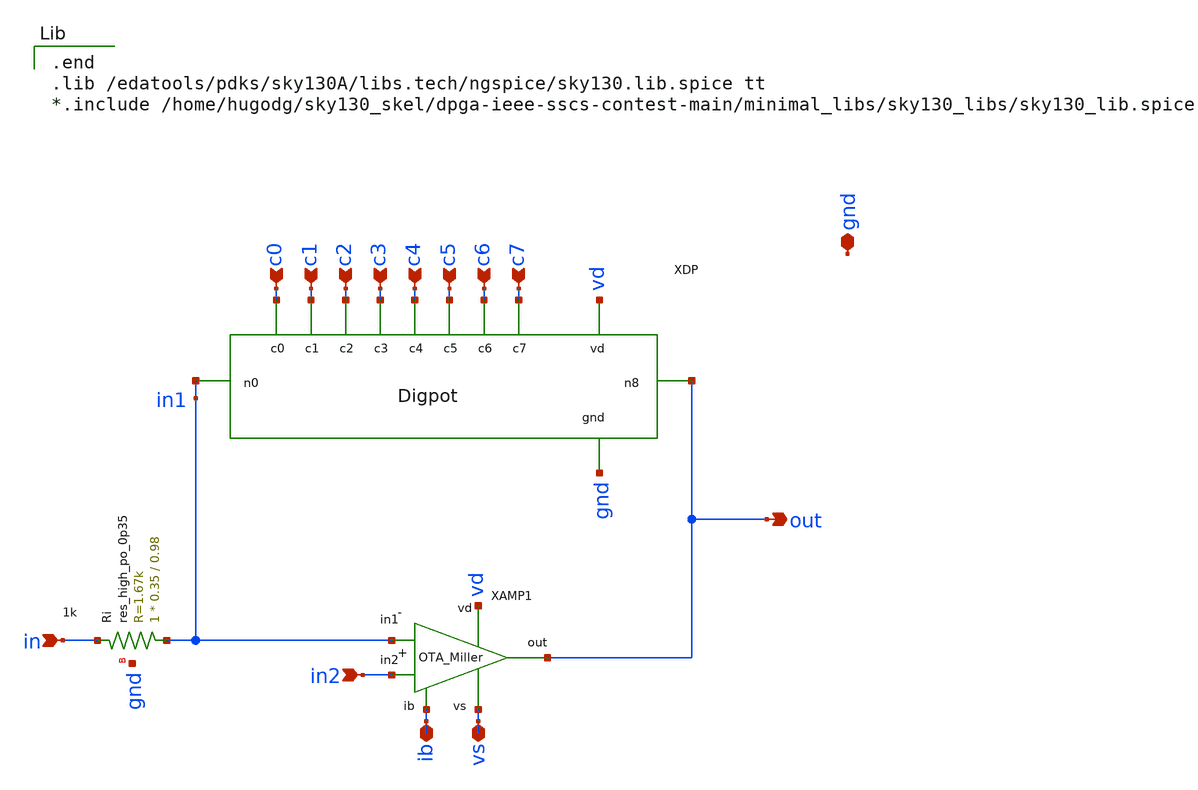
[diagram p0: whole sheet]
** sch_path: xschem/dpga.sch
* xschem/ota.sch:
* Copyright 2020 Stefan Frederik Schippers
* Licensed under the Apache License, Version 2.0 (the "License");
**.subckt dpga in in2 ib vs out gnd c0 c1 c2 c3 c4 c5 c6 c7
*.ipin in
*.ipin in2
*.iopin ib
*.iopin vs
*.opin out
*.iopin gnd
*.ipin c0
*.ipin c1
*.ipin c2
*.ipin c3
*.ipin c4
*.ipin c5
*.ipin c6
*.ipin c7
XDP1 gnd vd c5 c1 c2 c6 c7 c3 c0 c4 out in1 digpot
XOTA1 vd ib out in2 in1 vs ota
XRi in1 in gnd sky130_fd_pr__res_high_po_0p35 L=0.98 mult=1 m=1
**** begin user architecture code

.end
.lib /edatools/pdks/sky130A/libs.tech/ngspice/sky130.lib.spice tt
*.include /home/hugodg/sky130_skel/dpga-ieee-sscs-contest-main/minimal_libs/sky130_libs/sky130_lib.spice

**** end user architecture code
**.ends

* expanding   symbol:  /home/hugodg/sky130_skel/dpga-ieee-sscs-contest-main/xschem/digpot.sym # of
*+ pins=12
** sym_path: xschem/digpot.sym
** sch_path: xschem/digpot.sch
.subckt digpot gnd vd c5 c1 c2 c6 c7 c3 c0 c4 n8 n0
*.ipin c0
*.ipin c1
*.ipin c2
*.ipin c3
*.ipin c4
*.ipin c5
*.ipin c6
*.ipin c7
*.iopin gnd
*.iopin vd
*.iopin n0
*.iopin n8
xtg1 c0 vd n1 gnd n0 tg
xtg2 c1 vd n2 gnd n1 tg
xtg3 c2 vd n3 gnd n2 tg
xtg4 c3 vd n4 gnd n3 tg
xtg5 c4 vd n5 gnd n4 tg
xtg6 c5 vd n6 gnd n5 tg
xtg7 c6 vd n7 gnd n6 tg
xtg8 c7 vd n8 gnd n7 tg
XR0 n1 n0 gnd sky130_fd_pr__res_high_po_0p35 L=0.98 mult=1 m=1
XR1 n2 n1 gnd sky130_fd_pr__res_high_po_0p35 L=2.07 mult=1 m=1
XR2 n3 n2 gnd sky130_fd_pr__res_xhigh_po_0p35 L=0.58 mult=1 m=1
XR3 n4 n3 gnd sky130_fd_pr__res_xhigh_po_0p35 L=1.28 mult=1 m=1
XR4 n5 n4 gnd sky130_fd_pr__res_xhigh_po_0p35 L=2.68 mult=1 m=1
XR5 n6 n5 gnd sky130_fd_pr__res_xhigh_po_0p35 L=5.48 mult=1 m=1
XR6 n7 n6 gnd sky130_fd_pr__res_xhigh_po_0p35 L=10.73 mult=1 m=1
XR7 n8 n7 gnd sky130_fd_pr__res_xhigh_po_0p35 L=22.28 mult=1 m=1
.ends


* expanding   symbol:  /home/hugodg/sky130_skel/dpga-ieee-sscs-contest-main/xschem/ota.sym # of
*+ pins=6
** sym_path: xschem/ota.sym
** sch_path: xschem/ota.sch
.subckt ota vd ib out in2 in1 vs
*.iopin vd
*.iopin vs
*.iopin ib
*.ipin in1
*.ipin in2
*.opin out
XM4 d c vs vs sky130_fd_pr__nfet_01v8 L=1 W=0.861 nf=1 ad='int((nf+1)/2) * W/nf * 0.29' as='int((nf+2)/2) * W/nf * 0.29'
+ pd='2*int((nf+1)/2) * (W/nf + 0.29)' ps='2*int((nf+2)/2) * (W/nf + 0.29)' nrd='0.29 / W' nrs='0.29 / W'
+ sa=0 sb=0 sd=0 mult=1 m=1
XM7 e d vs vs sky130_fd_pr__nfet_01v8 L=1 W=8.61 nf=2 ad='int((nf+1)/2) * W/nf * 0.29' as='int((nf+2)/2) * W/nf * 0.29'
+ pd='2*int((nf+1)/2) * (W/nf + 0.29)' ps='2*int((nf+2)/2) * (W/nf + 0.29)' nrd='0.29 / W' nrs='0.29 / W'
+ sa=0 sb=0 sd=0 mult=1 m=1
XM5 ib ib vd vd sky130_fd_pr__pfet_01v8 L=1 W=5.85 nf=1 ad='int((nf+1)/2) * W/nf * 0.29' as='int((nf+2)/2) * W/nf * 0.29'
+ pd='2*int((nf+1)/2) * (W/nf + 0.29)' ps='2*int((nf+2)/2) * (W/nf + 0.29)' nrd='0.29 / W' nrs='0.29 / W'
+ sa=0 sb=0 sd=0 mult=1 m=1
XM6 b ib vd vd sky130_fd_pr__pfet_01v8 L=1 W=5.85 nf=1 ad='int((nf+1)/2) * W/nf * 0.29' as='int((nf+2)/2) * W/nf * 0.29'
+ pd='2*int((nf+1)/2) * (W/nf + 0.29)' ps='2*int((nf+2)/2) * (W/nf + 0.29)' nrd='0.29 / W' nrs='0.29 / W'
+ sa=0 sb=0 sd=0 mult=1 m=1
XM8 e ib vd vd sky130_fd_pr__pfet_01v8 L=1 W=29.3 nf=5 ad='int((nf+1)/2) * W/nf * 0.29' as='int((nf+2)/2) * W/nf * 0.29'
+ pd='2*int((nf+1)/2) * (W/nf + 0.29)' ps='2*int((nf+2)/2) * (W/nf + 0.29)' nrd='0.29 / W' nrs='0.29 / W'
+ sa=0 sb=0 sd=0 mult=1 m=1
XM10 out ib vd vd sky130_fd_pr__pfet_01v8 L=1 W=5.85 nf=1 ad='int((nf+1)/2) * W/nf * 0.29' as='int((nf+2)/2) * W/nf * 0.29'
+ pd='2*int((nf+1)/2) * (W/nf + 0.29)' ps='2*int((nf+2)/2) * (W/nf + 0.29)' nrd='0.29 / W' nrs='0.29 / W'
+ sa=0 sb=0 sd=0 mult=1 m=1
XM9 vs e out out sky130_fd_pr__pfet_01v8 L=1 W=5.85 nf=1 ad='int((nf+1)/2) * W/nf * 0.29' as='int((nf+2)/2) * W/nf * 0.29'
+ pd='2*int((nf+1)/2) * (W/nf + 0.29)' ps='2*int((nf+2)/2) * (W/nf + 0.29)' nrd='0.29 / W' nrs='0.29 / W'
+ sa=0 sb=0 sd=0 mult=1 m=1
XM1 c in1 b b sky130_fd_pr__pfet_01v8 L=1 W=2.93 nf=1 ad='int((nf+1)/2) * W/nf * 0.29' as='int((nf+2)/2) * W/nf * 0.29'
+ pd='2*int((nf+1)/2) * (W/nf + 0.29)' ps='2*int((nf+2)/2) * (W/nf + 0.29)' nrd='0.29 / W' nrs='0.29 / W'
+ sa=0 sb=0 sd=0 mult=1 m=1
XM2 d in2 b b sky130_fd_pr__pfet_01v8 L=1 W=2.93 nf=1 ad='int((nf+1)/2) * W/nf * 0.29' as='int((nf+2)/2) * W/nf * 0.29'
+ pd='2*int((nf+1)/2) * (W/nf + 0.29)' ps='2*int((nf+2)/2) * (W/nf + 0.29)' nrd='0.29 / W' nrs='0.29 / W'
+ sa=0 sb=0 sd=0 mult=1 m=1
XM3 c c vs vs sky130_fd_pr__nfet_01v8 L=1 W=0.861 nf=1 ad='int((nf+1)/2) * W/nf * 0.29' as='int((nf+2)/2) * W/nf * 0.29'
+ pd='2*int((nf+1)/2) * (W/nf + 0.29)' ps='2*int((nf+2)/2) * (W/nf + 0.29)' nrd='0.29 / W' nrs='0.29 / W'
+ sa=0 sb=0 sd=0 mult=1 m=1
XCC e d sky130_fd_pr__cap_mim_m3_1 W=22.023 L=22.023 MF=1 m=1
.ends


* expanding   symbol:  /home/hugodg/sky130_skel/dpga-ieee-sscs-contest-main/xschem/tg.sym # of
*+ pins=5
** sym_path: xschem/tg.sym
** sch_path: xschem/tg.sch
.subckt tg ctrl vd b vgnd a
*.iopin vd
*.iopin vgnd
*.iopin b
*.iopin a
*.ipin ctrl
XM2 a ctrl b b sky130_fd_pr__pfet_01v8 L=0.15 W=3 nf=1 ad='int((nf+1)/2) * W/nf * 0.29' as='int((nf+2)/2) * W/nf * 0.29'
+ pd='2*int((nf+1)/2) * (W/nf + 0.29)' ps='2*int((nf+2)/2) * (W/nf + 0.29)' nrd='0.29 / W' nrs='0.29 / W'
+ sa=0 sb=0 sd=0 mult=1 m=1
XM1 b nctrl net1 net1 sky130_fd_pr__nfet_01v8 L=0.15 W=1 nf=1 ad='int((nf+1)/2) * W/nf * 0.29' as='int((nf+2)/2) * W/nf * 0.29'
+ pd='2*int((nf+1)/2) * (W/nf + 0.29)' ps='2*int((nf+2)/2) * (W/nf + 0.29)' nrd='0.29 / W' nrs='0.29 / W'
+ sa=0 sb=0 sd=0 mult=1 m=1
XM3 nctrl ctrl vgnd vgnd sky130_fd_pr__nfet_01v8 L=0.15 W=1 nf=1 ad='int((nf+1)/2) * W/nf * 0.29' as='int((nf+2)/2) * W/nf * 0.29'
+ pd='2*int((nf+1)/2) * (W/nf + 0.29)' ps='2*int((nf+2)/2) * (W/nf + 0.29)' nrd='0.29 / W' nrs='0.29 / W'
+ sa=0 sb=0 sd=0 mult=1 m=1
XM4 nctrl ctrl vd vd sky130_fd_pr__pfet_01v8 L=0.15 W=3 nf=1 ad='int((nf+1)/2) * W/nf * 0.29' as='int((nf+2)/2) * W/nf * 0.29'
+ pd='2*int((nf+1)/2) * (W/nf + 0.29)' ps='2*int((nf+2)/2) * (W/nf + 0.29)' nrd='0.29 / W' nrs='0.29 / W'
+ sa=0 sb=0 sd=0 mult=1 m=1
.ends

.end
